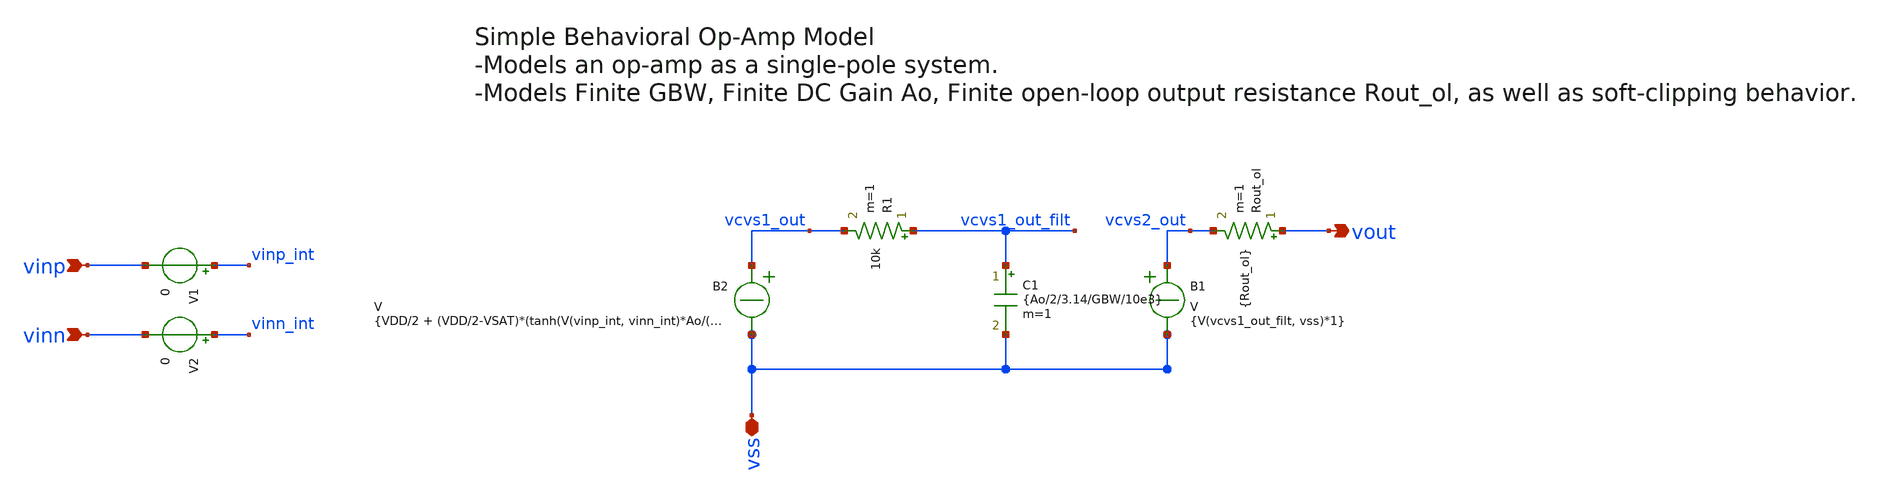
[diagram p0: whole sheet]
** sch_path: xsch/behavioral/ota.sch
**.subckt ota vinp vinn vout vss
*.ipin vinp
*.ipin vinn
*.opin vout
*.iopin vss
R1 vcvs1_out_filt vcvs1_out 10k m=1
C1 vcvs1_out_filt vss {Ao/2/3.14/GBW/10e3} m=1
Rout_ol vout vcvs2_out {Rout_ol} m=1
V1 vinp_int vinp 0
V2 vinn_int vinn 0
B2 vcvs1_out vss V = {VDD/2 + (VDD/2-VSAT)*(tanh(V(vinp_int, vinn_int)*Ao/(VDD/2-VSAT)))}
B1 vcvs2_out vss V = {V(vcvs1_out_filt, vss)*1}
**.ends
.end
